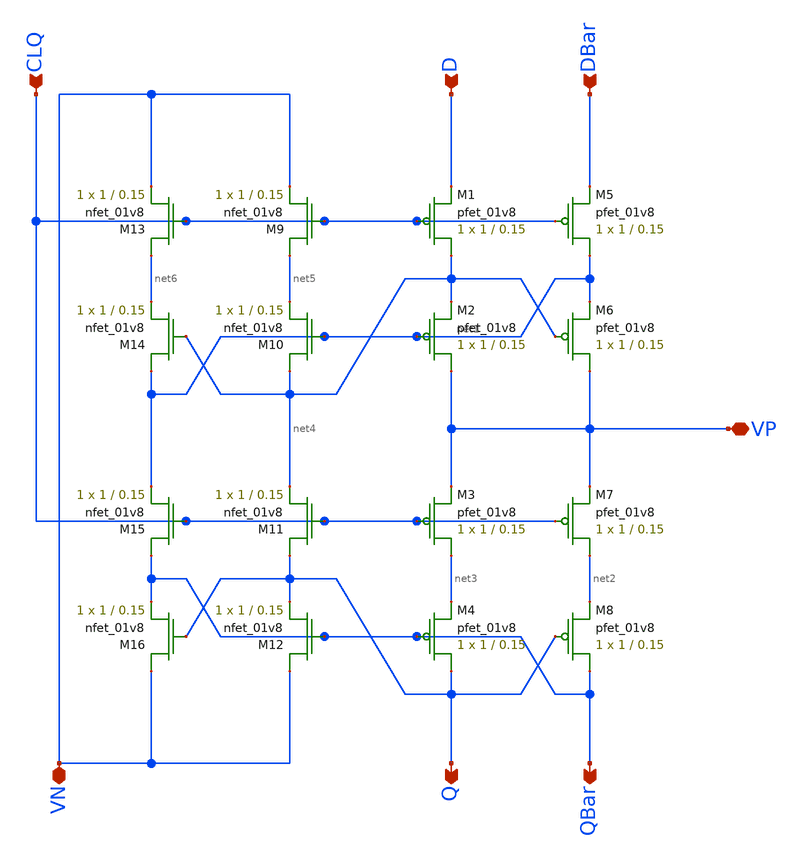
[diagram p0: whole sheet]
** sch_path: MADVLSI_MP2/old/CSRL_D_FF_3.sch
**.subckt CSRL_D_FF_3 D DBar CLQ VP VN Q QBar
*.ipin D
*.ipin DBar
*.ipin CLQ
*.iopin VP
*.iopin VN
*.opin Q
*.opin QBar
XM1 net4 CLQ D VDD sky130_fd_pr__pfet_01v8 L=0.15 W=1 nf=1 ad='int((nf+1)/2) * W/nf * 0.29' as='int((nf+2)/2) * W/nf * 0.29'
+ pd='2*int((nf+1)/2) * (W/nf + 0.29)' ps='2*int((nf+2)/2) * (W/nf + 0.29)' nrd='0.29 / W' nrs='0.29 / W'
+ sa=0 sb=0 sd=0 mult=1 m=1
XM2 VP net1 net4 VDD sky130_fd_pr__pfet_01v8 L=0.15 W=1 nf=1 ad='int((nf+1)/2) * W/nf * 0.29' as='int((nf+2)/2) * W/nf * 0.29'
+ pd='2*int((nf+1)/2) * (W/nf + 0.29)' ps='2*int((nf+2)/2) * (W/nf + 0.29)' nrd='0.29 / W' nrs='0.29 / W'
+ sa=0 sb=0 sd=0 mult=1 m=1
XM3 net3 CLQ VP VDD sky130_fd_pr__pfet_01v8 L=0.15 W=1 nf=1 ad='int((nf+1)/2) * W/nf * 0.29' as='int((nf+2)/2) * W/nf * 0.29'
+ pd='2*int((nf+1)/2) * (W/nf + 0.29)' ps='2*int((nf+2)/2) * (W/nf + 0.29)' nrd='0.29 / W' nrs='0.29 / W'
+ sa=0 sb=0 sd=0 mult=1 m=1
XM4 Q QBar net3 VDD sky130_fd_pr__pfet_01v8 L=0.15 W=1 nf=1 ad='int((nf+1)/2) * W/nf * 0.29' as='int((nf+2)/2) * W/nf * 0.29'
+ pd='2*int((nf+1)/2) * (W/nf + 0.29)' ps='2*int((nf+2)/2) * (W/nf + 0.29)' nrd='0.29 / W' nrs='0.29 / W'
+ sa=0 sb=0 sd=0 mult=1 m=1
XM5 net1 CLQ DBar VDD sky130_fd_pr__pfet_01v8 L=0.15 W=1 nf=1 ad='int((nf+1)/2) * W/nf * 0.29' as='int((nf+2)/2) * W/nf * 0.29'
+ pd='2*int((nf+1)/2) * (W/nf + 0.29)' ps='2*int((nf+2)/2) * (W/nf + 0.29)' nrd='0.29 / W' nrs='0.29 / W'
+ sa=0 sb=0 sd=0 mult=1 m=1
XM6 VP net4 net1 VDD sky130_fd_pr__pfet_01v8 L=0.15 W=1 nf=1 ad='int((nf+1)/2) * W/nf * 0.29' as='int((nf+2)/2) * W/nf * 0.29'
+ pd='2*int((nf+1)/2) * (W/nf + 0.29)' ps='2*int((nf+2)/2) * (W/nf + 0.29)' nrd='0.29 / W' nrs='0.29 / W'
+ sa=0 sb=0 sd=0 mult=1 m=1
XM7 net2 CLQ VP VDD sky130_fd_pr__pfet_01v8 L=0.15 W=1 nf=1 ad='int((nf+1)/2) * W/nf * 0.29' as='int((nf+2)/2) * W/nf * 0.29'
+ pd='2*int((nf+1)/2) * (W/nf + 0.29)' ps='2*int((nf+2)/2) * (W/nf + 0.29)' nrd='0.29 / W' nrs='0.29 / W'
+ sa=0 sb=0 sd=0 mult=1 m=1
XM8 QBar Q net2 VDD sky130_fd_pr__pfet_01v8 L=0.15 W=1 nf=1 ad='int((nf+1)/2) * W/nf * 0.29' as='int((nf+2)/2) * W/nf * 0.29'
+ pd='2*int((nf+1)/2) * (W/nf + 0.29)' ps='2*int((nf+2)/2) * (W/nf + 0.29)' nrd='0.29 / W' nrs='0.29 / W'
+ sa=0 sb=0 sd=0 mult=1 m=1
XM9 net5 CLQ VN GND sky130_fd_pr__nfet_01v8 L=0.15 W=1 nf=1 ad='int((nf+1)/2) * W/nf * 0.29' as='int((nf+2)/2) * W/nf * 0.29'
+ pd='2*int((nf+1)/2) * (W/nf + 0.29)' ps='2*int((nf+2)/2) * (W/nf + 0.29)' nrd='0.29 / W' nrs='0.29 / W'
+ sa=0 sb=0 sd=0 mult=1 m=1
XM10 net4 net1 net5 GND sky130_fd_pr__nfet_01v8 L=0.15 W=1 nf=1 ad='int((nf+1)/2) * W/nf * 0.29' as='int((nf+2)/2) * W/nf * 0.29'
+ pd='2*int((nf+1)/2) * (W/nf + 0.29)' ps='2*int((nf+2)/2) * (W/nf + 0.29)' nrd='0.29 / W' nrs='0.29 / W'
+ sa=0 sb=0 sd=0 mult=1 m=1
XM11 Q CLQ net4 GND sky130_fd_pr__nfet_01v8 L=0.15 W=1 nf=1 ad='int((nf+1)/2) * W/nf * 0.29' as='int((nf+2)/2) * W/nf * 0.29'
+ pd='2*int((nf+1)/2) * (W/nf + 0.29)' ps='2*int((nf+2)/2) * (W/nf + 0.29)' nrd='0.29 / W' nrs='0.29 / W'
+ sa=0 sb=0 sd=0 mult=1 m=1
XM12 VN QBar Q GND sky130_fd_pr__nfet_01v8 L=0.15 W=1 nf=1 ad='int((nf+1)/2) * W/nf * 0.29' as='int((nf+2)/2) * W/nf * 0.29'
+ pd='2*int((nf+1)/2) * (W/nf + 0.29)' ps='2*int((nf+2)/2) * (W/nf + 0.29)' nrd='0.29 / W' nrs='0.29 / W'
+ sa=0 sb=0 sd=0 mult=1 m=1
XM13 net6 CLQ VN GND sky130_fd_pr__nfet_01v8 L=0.15 W=1 nf=1 ad='int((nf+1)/2) * W/nf * 0.29' as='int((nf+2)/2) * W/nf * 0.29'
+ pd='2*int((nf+1)/2) * (W/nf + 0.29)' ps='2*int((nf+2)/2) * (W/nf + 0.29)' nrd='0.29 / W' nrs='0.29 / W'
+ sa=0 sb=0 sd=0 mult=1 m=1
XM14 net1 net4 net6 GND sky130_fd_pr__nfet_01v8 L=0.15 W=1 nf=1 ad='int((nf+1)/2) * W/nf * 0.29' as='int((nf+2)/2) * W/nf * 0.29'
+ pd='2*int((nf+1)/2) * (W/nf + 0.29)' ps='2*int((nf+2)/2) * (W/nf + 0.29)' nrd='0.29 / W' nrs='0.29 / W'
+ sa=0 sb=0 sd=0 mult=1 m=1
XM15 QBar CLQ net1 GND sky130_fd_pr__nfet_01v8 L=0.15 W=1 nf=1 ad='int((nf+1)/2) * W/nf * 0.29' as='int((nf+2)/2) * W/nf * 0.29'
+ pd='2*int((nf+1)/2) * (W/nf + 0.29)' ps='2*int((nf+2)/2) * (W/nf + 0.29)' nrd='0.29 / W' nrs='0.29 / W'
+ sa=0 sb=0 sd=0 mult=1 m=1
XM16 VN Q QBar GND sky130_fd_pr__nfet_01v8 L=0.15 W=1 nf=1 ad='int((nf+1)/2) * W/nf * 0.29' as='int((nf+2)/2) * W/nf * 0.29'
+ pd='2*int((nf+1)/2) * (W/nf + 0.29)' ps='2*int((nf+2)/2) * (W/nf + 0.29)' nrd='0.29 / W' nrs='0.29 / W'
+ sa=0 sb=0 sd=0 mult=1 m=1
**.ends
.end
